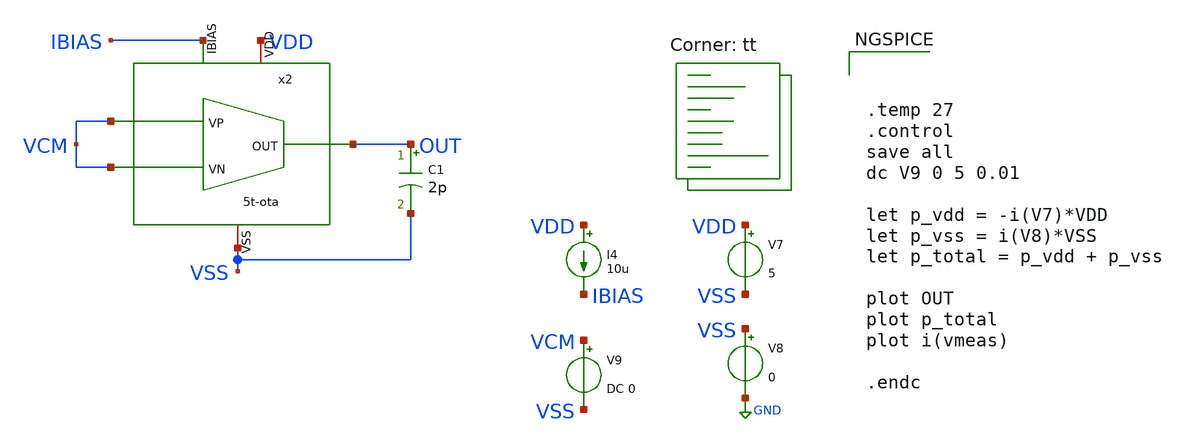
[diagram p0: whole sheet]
** sch_path: xschem/5t-ota/testbench/ICMR.sch
**.subckt ICMR
V7 VDD VSS 5
V8 VSS GND 0
I4 VDD IBIAS 10u
C1 OUT VSS 2p m=1
x2 VDD OUT IBIAS VCM VCM VSS 5t-ota
V9 VCM VSS DC 0
**** begin user architecture code



.temp 27
.control
save all
dc V9 0 5 0.01

let p_vdd = -i(V7)*VDD
let p_vss = i(V8)*VSS
let p_total = p_vdd + p_vss

plot OUT
plot p_total
plot i(vmeas)

.endc


.lib $::SKYWATER_MODELS/sky130.lib.spice tt
**** end user architecture code
**.ends

* expanding   symbol:  icdec-biomedical-pmic/xschem/5t-ota/schematics/5t-ota.sym # of pins=6
** sym_path: xschem/5t-ota/schematics/5t-ota.sym
** sch_path: xschem/5t-ota/schematics/5t-ota.sch
.subckt 5t-ota VDD OUT IBIAS VN VP VSS
*.ipin VP
*.ipin VN
*.ipin IBIAS
*.iopin VDD
*.iopin VSS
*.opin OUT
XM1 net1 VP net2 VSS sky130_fd_pr__nfet_g5v0d10v5 L=0.75 W=8.5 nf=1 ad='int((nf+1)/2) * W/nf * 0.29'
+ as='int((nf+2)/2) * W/nf * 0.29' pd='2*int((nf+1)/2) * (W/nf + 0.29)' ps='2*int((nf+2)/2) * (W/nf + 0.29)'
+ nrd='0.29 / W' nrs='0.29 / W' sa=0 sb=0 sd=0 mult=1 m=1
XM2 OUT VN net2 VSS sky130_fd_pr__nfet_g5v0d10v5 L=0.75 W=8.5 nf=1 ad='int((nf+1)/2) * W/nf * 0.29' as='int((nf+2)/2) * W/nf * 0.29'
+ pd='2*int((nf+1)/2) * (W/nf + 0.29)' ps='2*int((nf+2)/2) * (W/nf + 0.29)' nrd='0.29 / W' nrs='0.29 / W'
+ sa=0 sb=0 sd=0 mult=1 m=1
XM3 net2 IBIAS VSS VSS sky130_fd_pr__nfet_g5v0d10v5 L=1.25 W=1.58 nf=1 ad='int((nf+1)/2) * W/nf * 0.29'
+ as='int((nf+2)/2) * W/nf * 0.29' pd='2*int((nf+1)/2) * (W/nf + 0.29)' ps='2*int((nf+2)/2) * (W/nf + 0.29)'
+ nrd='0.29 / W' nrs='0.29 / W' sa=0 sb=0 sd=0 mult=1 m=1
XM4 OUT net1 VDD VDD sky130_fd_pr__pfet_g5v0d10v5 L=1.25 W=4.85 nf=1 ad='int((nf+1)/2) * W/nf * 0.29'
+ as='int((nf+2)/2) * W/nf * 0.29' pd='2*int((nf+1)/2) * (W/nf + 0.29)' ps='2*int((nf+2)/2) * (W/nf + 0.29)'
+ nrd='0.29 / W' nrs='0.29 / W' sa=0 sb=0 sd=0 mult=1 m=1
XM5 net1 net1 VDD VDD sky130_fd_pr__pfet_g5v0d10v5 L=1.25 W=4.85 nf=1 ad='int((nf+1)/2) * W/nf * 0.29'
+ as='int((nf+2)/2) * W/nf * 0.29' pd='2*int((nf+1)/2) * (W/nf + 0.29)' ps='2*int((nf+2)/2) * (W/nf + 0.29)'
+ nrd='0.29 / W' nrs='0.29 / W' sa=0 sb=0 sd=0 mult=1 m=1
XM6 IBIAS IBIAS VSS VSS sky130_fd_pr__nfet_g5v0d10v5 L=1.25 W=1.58 nf=1 ad='int((nf+1)/2) * W/nf * 0.29'
+ as='int((nf+2)/2) * W/nf * 0.29' pd='2*int((nf+1)/2) * (W/nf + 0.29)' ps='2*int((nf+2)/2) * (W/nf + 0.29)'
+ nrd='0.29 / W' nrs='0.29 / W' sa=0 sb=0 sd=0 mult=1 m=1
.ends

.GLOBAL GND
.end
